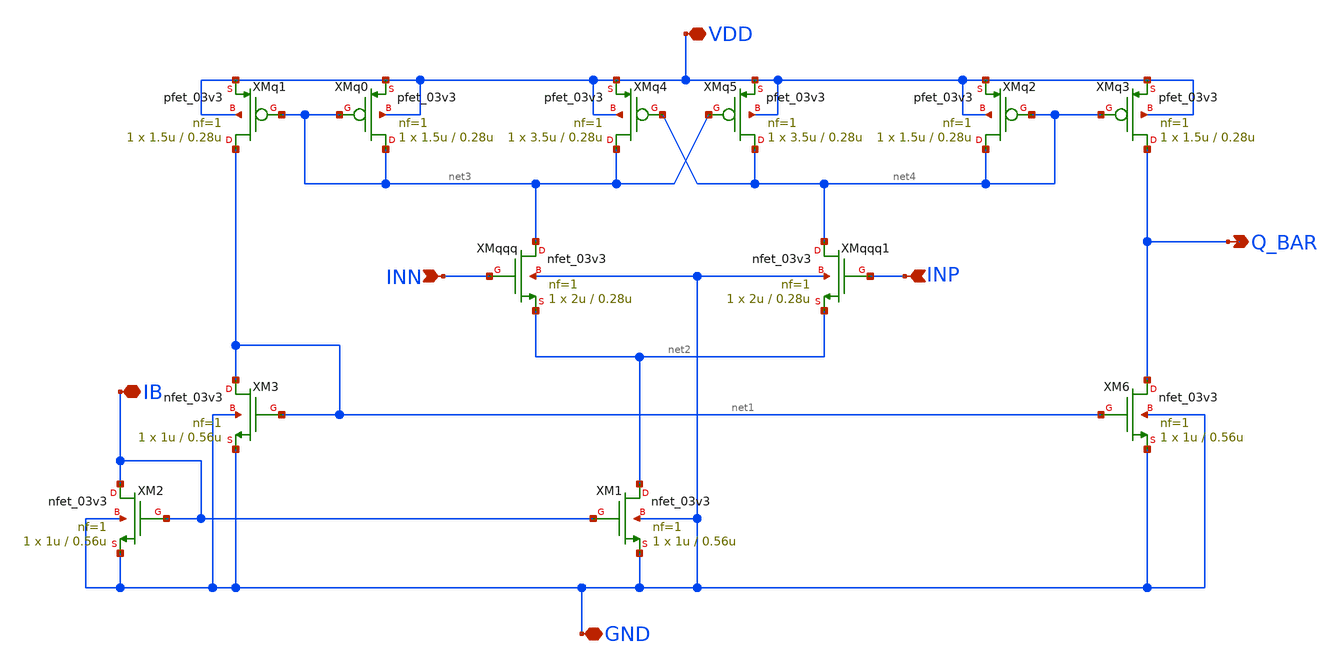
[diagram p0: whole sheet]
** sch_path: analog/B04_comparator.sch
**.subckt B04_comparator VDD GND INN INP IB Q_BAR
*.iopin VDD
*.iopin GND
*.ipin INN
*.ipin INP
*.iopin IB
*.opin Q_BAR
XM1 net2 IB GND GND nfet_03v3 L=0.56u W=1u nf=1 ad='int((nf+1)/2) * W/nf * 0.18u' as='int((nf+2)/2) * W/nf * 0.18u'
+ pd='2*int((nf+1)/2) * (W/nf + 0.18u)' ps='2*int((nf+2)/2) * (W/nf + 0.18u)' nrd='0.18u / W' nrs='0.18u / W'
+ sa=0 sb=0 sd=0 m=1
XM2 IB IB GND GND nfet_03v3 L=0.56u W=1u nf=1 ad='int((nf+1)/2) * W/nf * 0.18u' as='int((nf+2)/2) * W/nf * 0.18u'
+ pd='2*int((nf+1)/2) * (W/nf + 0.18u)' ps='2*int((nf+2)/2) * (W/nf + 0.18u)' nrd='0.18u / W' nrs='0.18u / W'
+ sa=0 sb=0 sd=0 m=1
XM3 net1 net1 GND GND nfet_03v3 L=0.56u W=1u nf=1 ad='int((nf+1)/2) * W/nf * 0.18u' as='int((nf+2)/2) * W/nf * 0.18u'
+ pd='2*int((nf+1)/2) * (W/nf + 0.18u)' ps='2*int((nf+2)/2) * (W/nf + 0.18u)' nrd='0.18u / W' nrs='0.18u / W'
+ sa=0 sb=0 sd=0 m=1
XMqqq net3 INN net2 GND nfet_03v3 L=0.28u W=2u nf=1 ad='int((nf+1)/2) * W/nf * 0.18u' as='int((nf+2)/2) * W/nf * 0.18u'
+ pd='2*int((nf+1)/2) * (W/nf + 0.18u)' ps='2*int((nf+2)/2) * (W/nf + 0.18u)' nrd='0.18u / W' nrs='0.18u / W'
+ sa=0 sb=0 sd=0 m=1
XMqqq1 net4 INP net2 GND nfet_03v3 L=0.28u W=2u nf=1 ad='int((nf+1)/2) * W/nf * 0.18u' as='int((nf+2)/2) * W/nf * 0.18u'
+ pd='2*int((nf+1)/2) * (W/nf + 0.18u)' ps='2*int((nf+2)/2) * (W/nf + 0.18u)' nrd='0.18u / W' nrs='0.18u / W'
+ sa=0 sb=0 sd=0 m=1
XM6 Q_BAR net1 GND GND nfet_03v3 L=0.56u W=1u nf=1 ad='int((nf+1)/2) * W/nf * 0.18u' as='int((nf+2)/2) * W/nf * 0.18u'
+ pd='2*int((nf+1)/2) * (W/nf + 0.18u)' ps='2*int((nf+2)/2) * (W/nf + 0.18u)' nrd='0.18u / W' nrs='0.18u / W'
+ sa=0 sb=0 sd=0 m=1
XMq0 net3 net3 VDD VDD pfet_03v3 L=0.28u W=1.5u nf=1 ad='int((nf+1)/2) * W/nf * 0.18u' as='int((nf+2)/2) * W/nf * 0.18u'
+ pd='2*int((nf+1)/2) * (W/nf + 0.18u)' ps='2*int((nf+2)/2) * (W/nf + 0.18u)' nrd='0.18u / W' nrs='0.18u / W'
+ sa=0 sb=0 sd=0 m=1
XMq1 net1 net3 VDD VDD pfet_03v3 L=0.28u W=1.5u nf=1 ad='int((nf+1)/2) * W/nf * 0.18u' as='int((nf+2)/2) * W/nf * 0.18u'
+ pd='2*int((nf+1)/2) * (W/nf + 0.18u)' ps='2*int((nf+2)/2) * (W/nf + 0.18u)' nrd='0.18u / W' nrs='0.18u / W'
+ sa=0 sb=0 sd=0 m=1
XMq4 net3 net4 VDD VDD pfet_03v3 L=0.28u W=3.5u nf=1 ad='int((nf+1)/2) * W/nf * 0.18u' as='int((nf+2)/2) * W/nf * 0.18u'
+ pd='2*int((nf+1)/2) * (W/nf + 0.18u)' ps='2*int((nf+2)/2) * (W/nf + 0.18u)' nrd='0.18u / W' nrs='0.18u / W'
+ sa=0 sb=0 sd=0 m=1
XMq5 net4 net3 VDD VDD pfet_03v3 L=0.28u W=3.5u nf=1 ad='int((nf+1)/2) * W/nf * 0.18u' as='int((nf+2)/2) * W/nf * 0.18u'
+ pd='2*int((nf+1)/2) * (W/nf + 0.18u)' ps='2*int((nf+2)/2) * (W/nf + 0.18u)' nrd='0.18u / W' nrs='0.18u / W'
+ sa=0 sb=0 sd=0 m=1
XMq2 net4 net4 VDD VDD pfet_03v3 L=0.28u W=1.5u nf=1 ad='int((nf+1)/2) * W/nf * 0.18u' as='int((nf+2)/2) * W/nf * 0.18u'
+ pd='2*int((nf+1)/2) * (W/nf + 0.18u)' ps='2*int((nf+2)/2) * (W/nf + 0.18u)' nrd='0.18u / W' nrs='0.18u / W'
+ sa=0 sb=0 sd=0 m=1
XMq3 Q_BAR net4 VDD VDD pfet_03v3 L=0.28u W=1.5u nf=1 ad='int((nf+1)/2) * W/nf * 0.18u' as='int((nf+2)/2) * W/nf * 0.18u'
+ pd='2*int((nf+1)/2) * (W/nf + 0.18u)' ps='2*int((nf+2)/2) * (W/nf + 0.18u)' nrd='0.18u / W' nrs='0.18u / W'
+ sa=0 sb=0 sd=0 m=1
**.ends
.end
